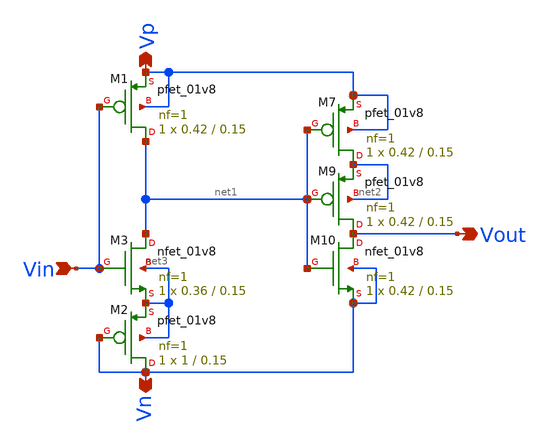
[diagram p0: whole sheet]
** sch_path: xschem/Vth_sch/Symbol/th10.sch
**.subckt th10 Vn Vp Vin Vout
*.opin Vn
*.opin Vp
*.ipin Vin
*.opin Vout
XM1 net1 Vin Vp Vp sky130_fd_pr__pfet_01v8 L=0.15 W=0.42 nf=1 ad='int((nf+1)/2) * W/nf * 0.29' as='int((nf+2)/2) * W/nf * 0.29'
+ pd='2*int((nf+1)/2) * (W/nf + 0.29)' ps='2*int((nf+2)/2) * (W/nf + 0.29)' nrd='0.29 / W' nrs='0.29 / W'
+ sa=0 sb=0 sd=0 mult=1 m=1
XM3 net1 Vin net3 net3 sky130_fd_pr__nfet_01v8 L=0.15 W=0.36 nf=1 ad='int((nf+1)/2) * W/nf * 0.29' as='int((nf+2)/2) * W/nf * 0.29'
+ pd='2*int((nf+1)/2) * (W/nf + 0.29)' ps='2*int((nf+2)/2) * (W/nf + 0.29)' nrd='0.29 / W' nrs='0.29 / W'
+ sa=0 sb=0 sd=0 mult=1 m=1
XM2 Vn Vn net3 net3 sky130_fd_pr__pfet_01v8 L=0.15 W=1 nf=1 ad='int((nf+1)/2) * W/nf * 0.29' as='int((nf+2)/2) * W/nf * 0.29'
+ pd='2*int((nf+1)/2) * (W/nf + 0.29)' ps='2*int((nf+2)/2) * (W/nf + 0.29)' nrd='0.29 / W' nrs='0.29 / W'
+ sa=0 sb=0 sd=0 mult=1 m=1
XM7 net2 net1 Vp Vp sky130_fd_pr__pfet_01v8 L=0.15 W=0.42 nf=1 ad='int((nf+1)/2) * W/nf * 0.29' as='int((nf+2)/2) * W/nf * 0.29'
+ pd='2*int((nf+1)/2) * (W/nf + 0.29)' ps='2*int((nf+2)/2) * (W/nf + 0.29)' nrd='0.29 / W' nrs='0.29 / W'
+ sa=0 sb=0 sd=0 mult=1 m=1
XM9 Vout net1 net2 net2 sky130_fd_pr__pfet_01v8 L=0.15 W=0.42 nf=1 ad='int((nf+1)/2) * W/nf * 0.29' as='int((nf+2)/2) * W/nf * 0.29'
+ pd='2*int((nf+1)/2) * (W/nf + 0.29)' ps='2*int((nf+2)/2) * (W/nf + 0.29)' nrd='0.29 / W' nrs='0.29 / W'
+ sa=0 sb=0 sd=0 mult=1 m=1
XM10 Vout net1 Vn Vn sky130_fd_pr__nfet_01v8 L=0.15 W=0.42 nf=1 ad='int((nf+1)/2) * W/nf * 0.29' as='int((nf+2)/2) * W/nf * 0.29'
+ pd='2*int((nf+1)/2) * (W/nf + 0.29)' ps='2*int((nf+2)/2) * (W/nf + 0.29)' nrd='0.29 / W' nrs='0.29 / W'
+ sa=0 sb=0 sd=0 mult=1 m=1
**.ends
.end
